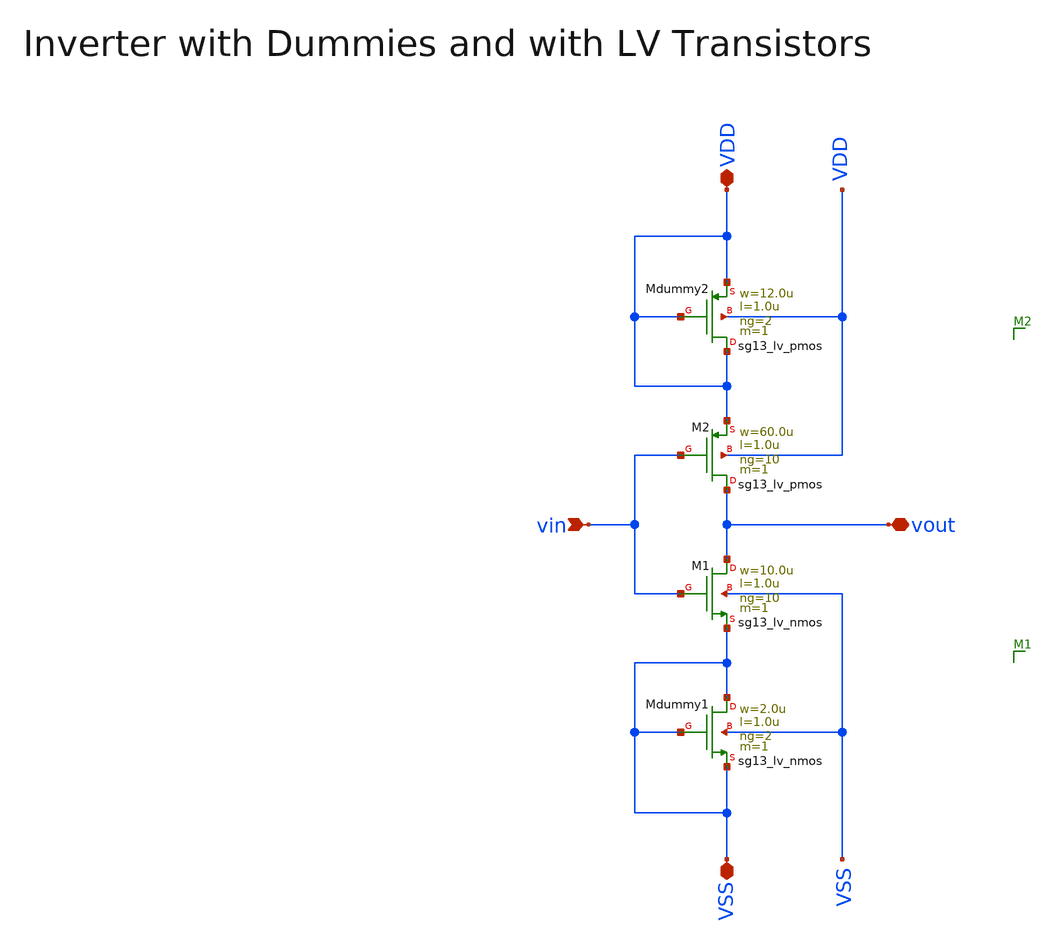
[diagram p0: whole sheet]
** sch_path: ihp130/macros/iqmod/schematic/xschem/iqmod_mfb_lpf_ota_core_inv_NF10.sch
**.subckt iqmod_mfb_lpf_ota_core_inv_NF10 vin VDD VSS vout
*.ipin vin
*.iopin VDD
*.iopin VSS
*.iopin vout
XM1 vout vin VSS VSS sg13_lv_nmos w=10.0u l=1.0u ng=10 m=1 mm_ok=1
XM2 vout vin VDD VDD sg13_lv_pmos w=60.0u l=1.0u ng=10 m=1 mm_ok=1
XMdummy1 VSS VSS VSS VSS sg13_lv_nmos w=2.0u l=1.0u ng=2 m=1 mm_ok=1
XMdummy2 VDD VDD VDD VDD sg13_lv_pmos w=12.0u l=1.0u ng=2 m=1 mm_ok=1
**.ends
.end
